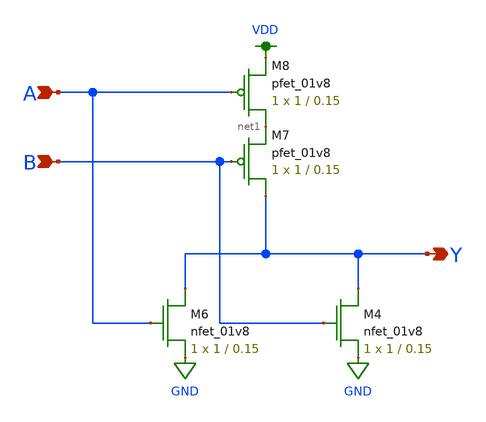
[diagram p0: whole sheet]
** sch_path: schematics/nor2.sch
**.subckt nor2 A B Y
*.ipin A
*.ipin B
*.opin Y
XM4 Y B GND GND sky130_fd_pr__nfet_01v8 L=0.15 W=1 nf=1 ad='int((nf+1)/2) * W/nf * 0.29' as='int((nf+2)/2) * W/nf * 0.29'
+ pd='2*int((nf+1)/2) * (W/nf + 0.29)' ps='2*int((nf+2)/2) * (W/nf + 0.29)' nrd='0.29 / W' nrs='0.29 / W'
+ sa=0 sb=0 sd=0 mult=1 m=1
XM6 Y A GND GND sky130_fd_pr__nfet_01v8 L=0.15 W=1 nf=1 ad='int((nf+1)/2) * W/nf * 0.29' as='int((nf+2)/2) * W/nf * 0.29'
+ pd='2*int((nf+1)/2) * (W/nf + 0.29)' ps='2*int((nf+2)/2) * (W/nf + 0.29)' nrd='0.29 / W' nrs='0.29 / W'
+ sa=0 sb=0 sd=0 mult=1 m=1
XM7 Y B net1 VDD sky130_fd_pr__pfet_01v8 L=0.15 W=1 nf=1 ad='int((nf+1)/2) * W/nf * 0.29' as='int((nf+2)/2) * W/nf * 0.29'
+ pd='2*int((nf+1)/2) * (W/nf + 0.29)' ps='2*int((nf+2)/2) * (W/nf + 0.29)' nrd='0.29 / W' nrs='0.29 / W'
+ sa=0 sb=0 sd=0 mult=1 m=1
XM8 net1 A VDD VDD sky130_fd_pr__pfet_01v8 L=0.15 W=1 nf=1 ad='int((nf+1)/2) * W/nf * 0.29' as='int((nf+2)/2) * W/nf * 0.29'
+ pd='2*int((nf+1)/2) * (W/nf + 0.29)' ps='2*int((nf+2)/2) * (W/nf + 0.29)' nrd='0.29 / W' nrs='0.29 / W'
+ sa=0 sb=0 sd=0 mult=1 m=1
**.ends
.GLOBAL VDD
.GLOBAL GND
.end
